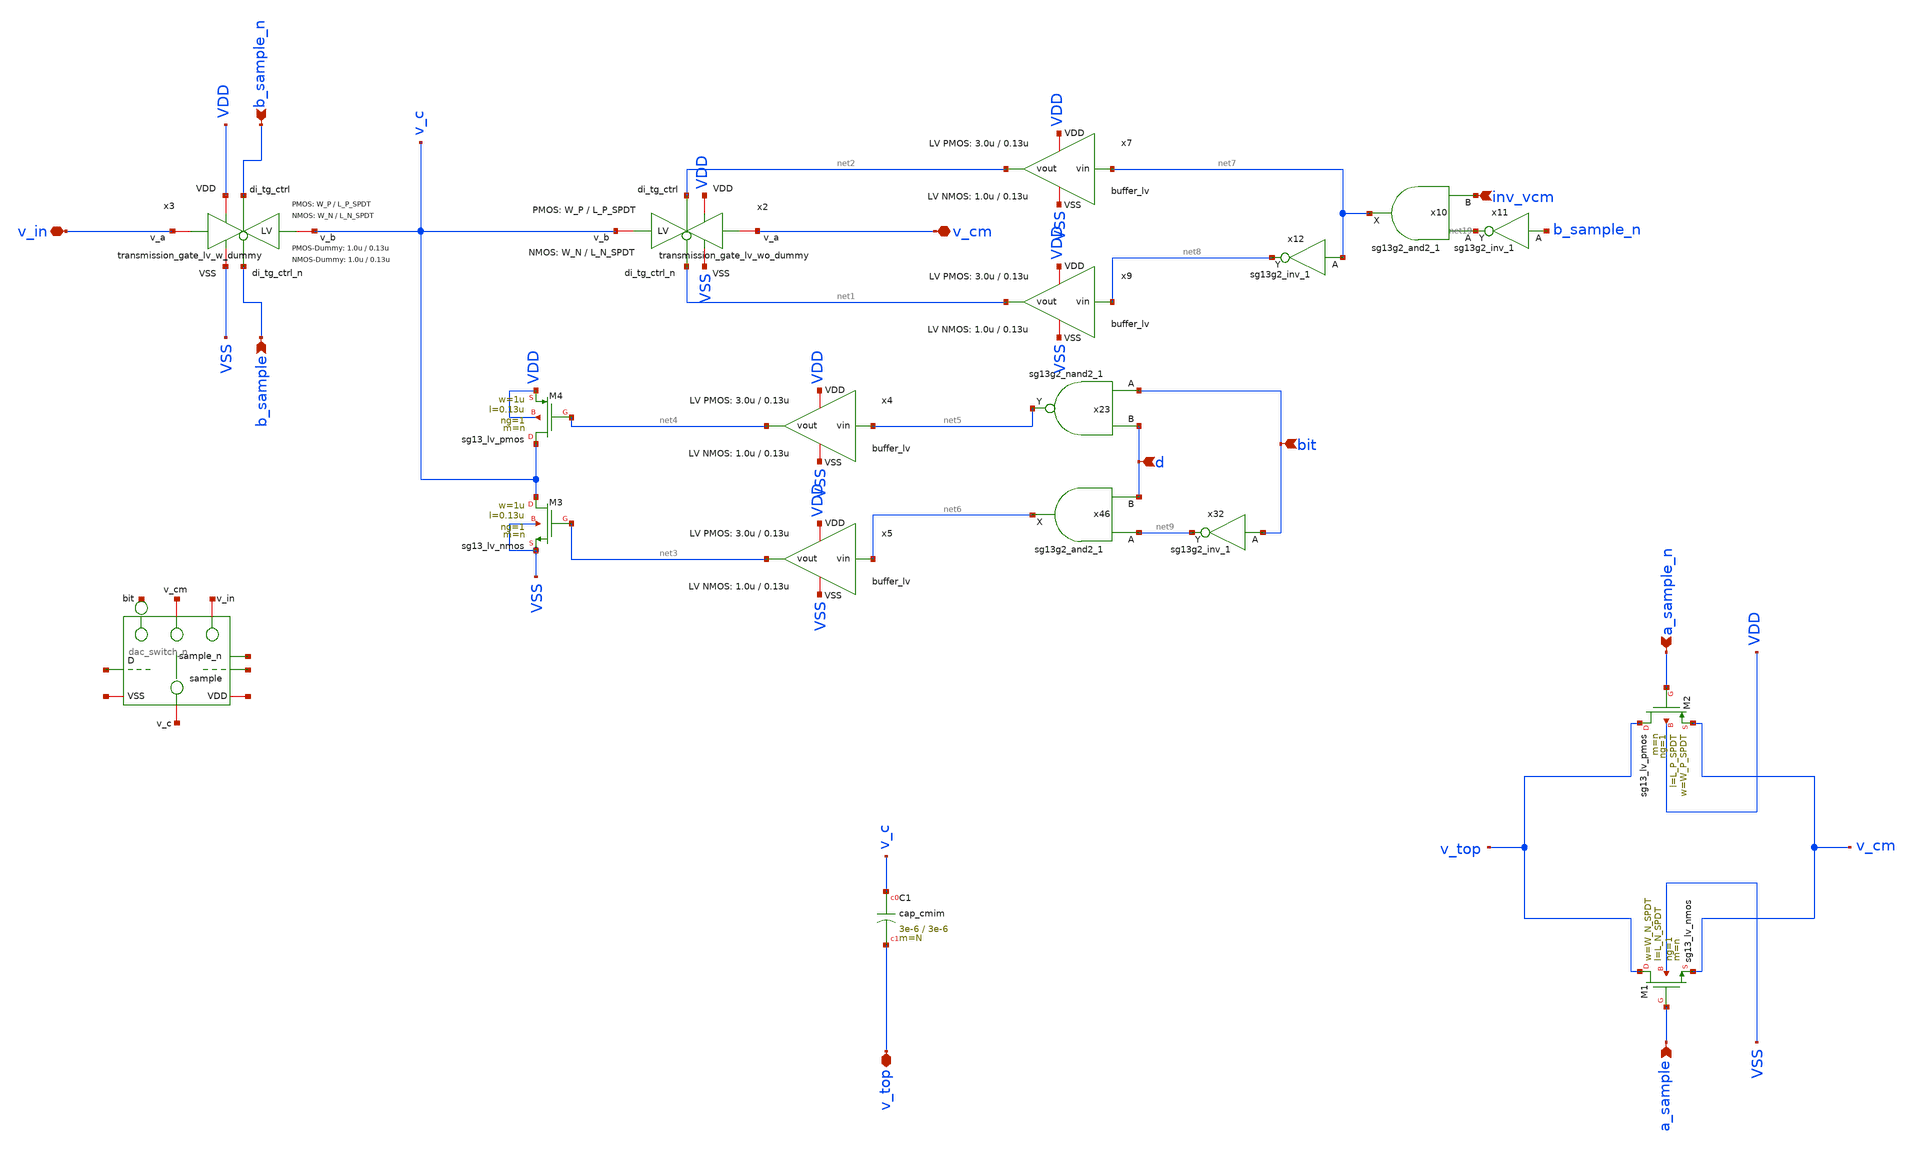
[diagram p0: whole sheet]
** sch_path: xschem/dac_icms_cell/unit_cell_n.sch
* IHP-GmbH/IHP-Open-PDK/ihp-sg13g2/libs.tech/xschem/sg13g2_stdcells/sg13g2_nor2_1.sch:
* Copyright 2023 IHP PDK Authors
* Licensed under the Apache License, Version 2.0 (the "License");
**.subckt unit_cell_n d v_top a_sample a_sample_n v_in v_cm bit b_sample_n b_sample inv_vcm
*.ipin d
*.iopin v_top
*.ipin a_sample
*.ipin a_sample_n
*.iopin v_in
*.iopin v_cm
*.ipin bit
*.ipin b_sample_n
*.ipin b_sample
*.ipin inv_vcm
x1 net10 net11 net12 net13 net14 net15 net16 net17 net18 dac_switch_n W_P_TG=3.0u L_P_TG=L_P_SPDT W_N_TG=1.0u
+ L_N_TG=L_N_SPDT n={N}
XC1 v_c v_top cap_cmim w=3e-6 l=3e-6 m=N mm_ok=1
XM1 v_top a_sample v_cm VSS sg13_lv_nmos w=W_N_SPDT l=L_N_SPDT ng=1 m=n mm_ok=1
XM2 v_top a_sample_n v_cm VDD sg13_lv_pmos w=W_P_SPDT l=L_P_SPDT ng=1 m=n mm_ok=1
XM3 v_c net3 VSS VSS sg13_lv_nmos w=1u l=0.13u ng=1 m=n mm_ok=1
XM4 v_c net4 VDD VDD sg13_lv_pmos w=1u l=0.13u ng=1 m=n mm_ok=1
x2 VDD net2 VSS v_c v_cm net1 transmission_gate_lv_wo_dummy W_P=W_P L_P=L_P_SPDT W_N=W_N
+ L_N=L_N_SPDT W_P_D=1.0u L_P_D=0.13u W_N_D=1.0u L_N_D=0.13u n=n
x3 VDD b_sample_n VSS v_c v_in b_sample transmission_gate_lv_w_dummy W_P=W_P L_P=L_P_SPDT W_N=W_N
+ L_N=L_N_SPDT W_P_D=1.0u L_P_D=0.13u W_N_D=1.0u L_N_D=0.13u n=n
x23 net5 bit d VDD VSS sg13g2_nand2_1
x46 net6 net9 d VDD VSS sg13g2_and2_1
x4 VDD net5 net4 VSS buffer_lv W_P_INV=3.0u L_P_INV=0.13u W_N_INV=1.0u L_N_INV=0.13u
x5 VDD net6 net3 VSS buffer_lv W_P_INV=3.0u L_P_INV=0.13u W_N_INV=1.0u L_N_INV=0.13u
x7 VDD net7 net2 VSS buffer_lv W_P_INV=3.0u L_P_INV=0.13u W_N_INV=1.0u L_N_INV=0.13u
x9 VDD net8 net1 VSS buffer_lv W_P_INV=3.0u L_P_INV=0.13u W_N_INV=1.0u L_N_INV=0.13u
x32 net9 bit VDD VSS sg13g2_inv_1
x10 net7 net19 inv_vcm VDD VSS sg13g2_and2_1
x11 net19 b_sample_n VDD VSS sg13g2_inv_1
x12 net8 net7 VDD VSS sg13g2_inv_1
**.ends

* expanding   symbol:  dac_icms_cell/dac_switch_n.sym # of pins=9
** sym_path: xschem/dac_icms_cell/dac_switch_n.sym
** sch_path: xschem/dac_icms_cell/dac_switch_n.sch
.subckt dac_switch_n VDD d VSS v_cap bit v_cm v_in sample sample_n  W_P_TG=3.0u L_P_TG=0.13u
+ W_N_TG=1.0u L_N_TG=0.13u n=1
*.iopin v_in
*.iopin v_cap
*.iopin VDD
*.iopin VSS
*.ipin d
*.iopin v_cm
*.ipin bit
*.ipin sample
*.ipin sample_n
x8 VDD d d_n VSS inverter_lv W_P=W_P_TG L_P=L_P_TG W_N=W_N_TG L_N=L_N_TG N_C=1
XM1 v_cap net3 VSS VSS sg13_lv_nmos w=1u l=0.2u ng=1 m=n mm_ok=1
XM3 v_cap net4 VDD VDD sg13_lv_pmos w=1.2u l=0.13u ng=1 m=n mm_ok=1
x2 VDD net2 VSS v_cap v_cm net1 transmission_gate_lv_w_dummy W_P=W_P_TG L_P=L_P_TG W_N=W_N_TG
+ L_N=L_N_TG W_P_D=1.0u L_P_D=0.13u W_N_D=1.0u L_N_D=0.13u n=n
x1 VDD sample VSS v_cap v_in sample_n transmission_gate_lv_w_dummy W_P=W_P_TG L_P=L_P_TG W_N=W_N_TG
+ L_N=L_N_TG W_P_D=1.0u L_P_D=0.13u W_N_D=1.0u L_N_D=0.13u n=n
x23 net5 bit d VDD VSS sg13g2_nand2_1
x46 net6 net9 d VDD VSS sg13g2_and2_1
x4 VDD net5 net4 VSS buffer_lv W_P_INV=3.0u L_P_INV=0.13u W_N_INV=1.0u L_N_INV=0.13u
x5 VDD net6 net3 VSS buffer_lv W_P_INV=3.0u L_P_INV=0.13u W_N_INV=1.0u L_N_INV=0.13u
x3 net7 d sample VDD VSS sg13g2_nor2_1
x6 net8 d sample VDD VSS sg13g2_or2_1
x7 VDD net7 net2 VSS buffer_lv W_P_INV=3.0u L_P_INV=0.13u W_N_INV=1.0u L_N_INV=0.13u
x9 VDD net8 net1 VSS buffer_lv W_P_INV=3.0u L_P_INV=0.13u W_N_INV=1.0u L_N_INV=0.13u
x32 net9 bit VDD VSS sg13g2_inv_1
.ends


* expanding   symbol:  transmission_gate/transmission_gate_lv_wo_dummy.sym # of pins=6
** sym_path: xschem/transmission_gate/transmission_gate_lv_wo_dummy.sym
** sch_path: xschem/transmission_gate/transmission_gate_lv_wo_dummy.sch
.subckt transmission_gate_lv_wo_dummy VDD di_tg_ctrl VSS v_b v_a di_tg_ctrl_n  W_P=2.0u L_P=0.13u
+ W_N=2.0u L_N=0.13u W_P_D=1.0u L_P_D=0.13u W_N_D=1.0u L_N_D=0.13u n=1
*.iopin v_a
*.iopin v_b
*.iopin VDD
*.iopin VSS
*.ipin di_tg_ctrl
*.ipin di_tg_ctrl_n
XM1 v_a di_tg_ctrl v_b VSS sg13_lv_nmos w=W_N l=L_N ng=1 m=n mm_ok=1
XM2 v_a di_tg_ctrl_n v_b VDD sg13_lv_pmos w=W_P l=L_P ng=1 m=n mm_ok=1
.ends


* expanding   symbol:  transmission_gate/transmission_gate_lv_w_dummy.sym # of pins=6
** sym_path: xschem/transmission_gate/transmission_gate_lv_w_dummy.sym
** sch_path: xschem/transmission_gate/transmission_gate_lv_w_dummy.sch
.subckt transmission_gate_lv_w_dummy VDD di_tg_ctrl VSS v_b v_a di_tg_ctrl_n  W_P=2.0u L_P=0.13u
+ W_N=2.0u L_N=0.13u W_P_D=1.0u L_P_D=0.13u W_N_D=1.0u L_N_D=0.13u n=1
*.iopin v_a
*.iopin v_b
*.iopin VDD
*.iopin VSS
*.ipin di_tg_ctrl
*.ipin di_tg_ctrl_n
XM1 v_a di_tg_ctrl v_b VSS sg13_lv_nmos w=W_N l=L_N ng=1 m=n mm_ok=1
XM2 v_a di_tg_ctrl_n v_b VDD sg13_lv_pmos w=W_P l=L_P ng=1 m=n mm_ok=1
XMdummy2 v_b di_tg_ctrl v_b VDD sg13_lv_pmos w=W_P l=L_P ng=1 m={n/2} mm_ok=1
XMdummy1 v_b di_tg_ctrl_n v_b VSS sg13_lv_nmos w=W_N l=L_N ng=1 m={n/2} mm_ok=1
.ends


* expanding   symbol:  sg13g2_stdcells/sg13g2_nand2_1.sym # of pins=3
** sym_path: sg13g2_stdcells/sg13g2_nand2_1.sym
** sch_path: sg13g2_stdcells/sg13g2_nand2_1.sch
.subckt sg13g2_nand2_1 Y A B VDD VSS
*.iopin VDD
*.iopin VSS
*.ipin A
*.ipin B
*.opin Y
XM1 Y A net1 VSS sg13_lv_nmos w=740.00n l=130.00n ng=1 m=1 mm_ok=1
XM2 net1 B VSS VSS sg13_lv_nmos w=740.00n l=130.00n ng=1 m=1 mm_ok=1
XM3 Y A VDD VDD sg13_lv_pmos w=1.12u l=130.00n ng=1 m=1 mm_ok=1
XM4 Y B VDD VDD sg13_lv_pmos w=1.12u l=130.00n ng=1 m=1 mm_ok=1
.ends


* expanding   symbol:  sg13g2_stdcells/sg13g2_and2_1.sym # of pins=3
** sym_path: sg13g2_stdcells/sg13g2_and2_1.sym
** sch_path: sg13g2_stdcells/sg13g2_and2_1.sch
.subckt sg13g2_and2_1 X A B VDD VSS
*.ipin A
*.ipin B
*.opin X
*.iopin VDD
*.iopin VSS
XM1 net1 A net2 VSS sg13_lv_nmos w=640.00n l=130.00n ng=1 m=1 mm_ok=1
XM2 net2 B VSS VSS sg13_lv_nmos w=640.00n l=130.00n ng=1 m=1 mm_ok=1
XM3 X net1 VSS VSS sg13_lv_nmos w=740.00n l=130.00n ng=1 m=1 mm_ok=1
XM4 net1 B VDD VDD sg13_lv_pmos w=840.00n l=130.00n ng=1 m=1 mm_ok=1
XM5 net1 A VDD VDD sg13_lv_pmos w=840.00n l=130.00n ng=1 m=1 mm_ok=1
XM6 X net1 VDD VDD sg13_lv_pmos w=1.12u l=130.00n ng=1 m=1 mm_ok=1
.ends


* expanding   symbol:  buffer/buffer_lv.sym # of pins=4
** sym_path: buffer/buffer_lv.sym
** sch_path: buffer/buffer_lv.sch
.subckt buffer_lv VDD vin vout VSS  W_P_INV=3.0u L_P_INV=0.13u W_N_INV=1.0u L_N_INV=0.13u
*.ipin vin
*.iopin VDD
*.iopin VSS
*.opin vout
x1 VDD vin net1 VSS inverter_lv W_P=W_P_INV L_P=L_P_INV W_N=W_N_INV L_N=L_N_INV N_C=1
x2 VDD net1 vout VSS inverter_lv W_P=W_P_INV L_P=L_P_INV W_N=W_N_INV L_N=L_N_INV N_C=1
.ends


* expanding   symbol:  sg13g2_stdcells/sg13g2_inv_1.sym # of pins=2
** sym_path: sg13g2_stdcells/sg13g2_inv_1.sym
** sch_path: sg13g2_stdcells/sg13g2_inv_1.sch
.subckt sg13g2_inv_1 Y A VDD VSS
*.opin Y
*.ipin A
*.iopin VDD
*.iopin VSS
XM1 Y A VSS VSS sg13_lv_nmos w=740.00n l=130.00n ng=1 m=1 mm_ok=1
XM2 Y A VDD VDD sg13_lv_pmos w=1.12u l=130.00n ng=1 m=1 mm_ok=1
.ends


* expanding   symbol:  inverter/inverter_lv.sym # of pins=4
** sym_path: xschem/inverter/inverter_lv.sym
** sch_path: xschem/inverter/inverter_lv.sch
.subckt inverter_lv VDD vin vout VSS  W_P=3.0u L_P=0.13u W_N=1.0u L_N=0.13u N_C=1
*.ipin vin
*.iopin VDD
*.iopin VSS
*.opin vout
XM1 vout vin VDD VDD sg13_lv_pmos w=W_P l=L_P ng=1 m={N_C} mm_ok=1
XM2 vout vin VSS VSS sg13_lv_nmos w=W_N l=L_N ng=1 m={N_C} mm_ok=1
.ends


* expanding   symbol:  sg13g2_stdcells/sg13g2_nor2_1.sym # of pins=3
** sym_path: sg13g2_stdcells/sg13g2_nor2_1.sym
** sch_path: sg13g2_stdcells/sg13g2_nor2_1.sch
.subckt sg13g2_nor2_1 Y A B VDD VSS
*.opin Y
*.ipin B
*.ipin A
*.iopin VDD
*.iopin VSS
XM1 Y A VSS VSS sg13_lv_nmos w=740.00n l=130.00n ng=1 m=1 mm_ok=1
XM2 Y B VSS VSS sg13_lv_nmos w=740.00n l=130.00n ng=1 m=1 mm_ok=1
XM3 net1 A VDD VDD sg13_lv_pmos w=1.12u l=130.00n ng=1 m=1 mm_ok=1
XM4 Y B net1 VDD sg13_lv_pmos w=1.12u l=130.00n ng=1 m=1 mm_ok=1
.ends


* expanding   symbol:  sg13g2_stdcells/sg13g2_or2_1.sym # of pins=3
** sym_path: sg13g2_stdcells/sg13g2_or2_1.sym
** sch_path: sg13g2_stdcells/sg13g2_or2_1.sch
.subckt sg13g2_or2_1 X A B VDD VSS
*.opin X
*.ipin B
*.ipin A
*.iopin VDD
*.iopin VSS
XM1 net1 B VSS VSS sg13_lv_nmos w=550.00n l=130.00n ng=1 m=1 mm_ok=1
XM2 net1 A VSS VSS sg13_lv_nmos w=550.00n l=130.00n ng=1 m=1 mm_ok=1
XM3 X net1 VSS VSS sg13_lv_nmos w=740.00n l=130.00n ng=1 m=1 mm_ok=1
XM4 net2 A VDD VDD sg13_lv_pmos w=840.00n l=130.00n ng=1 m=1 mm_ok=1
XM5 net1 B net2 VDD sg13_lv_pmos w=840.00n l=130.00n ng=1 m=1 mm_ok=1
XM6 X net1 VDD VDD sg13_lv_pmos w=1.12u l=130.00n ng=1 m=1 mm_ok=1
.ends

.end
